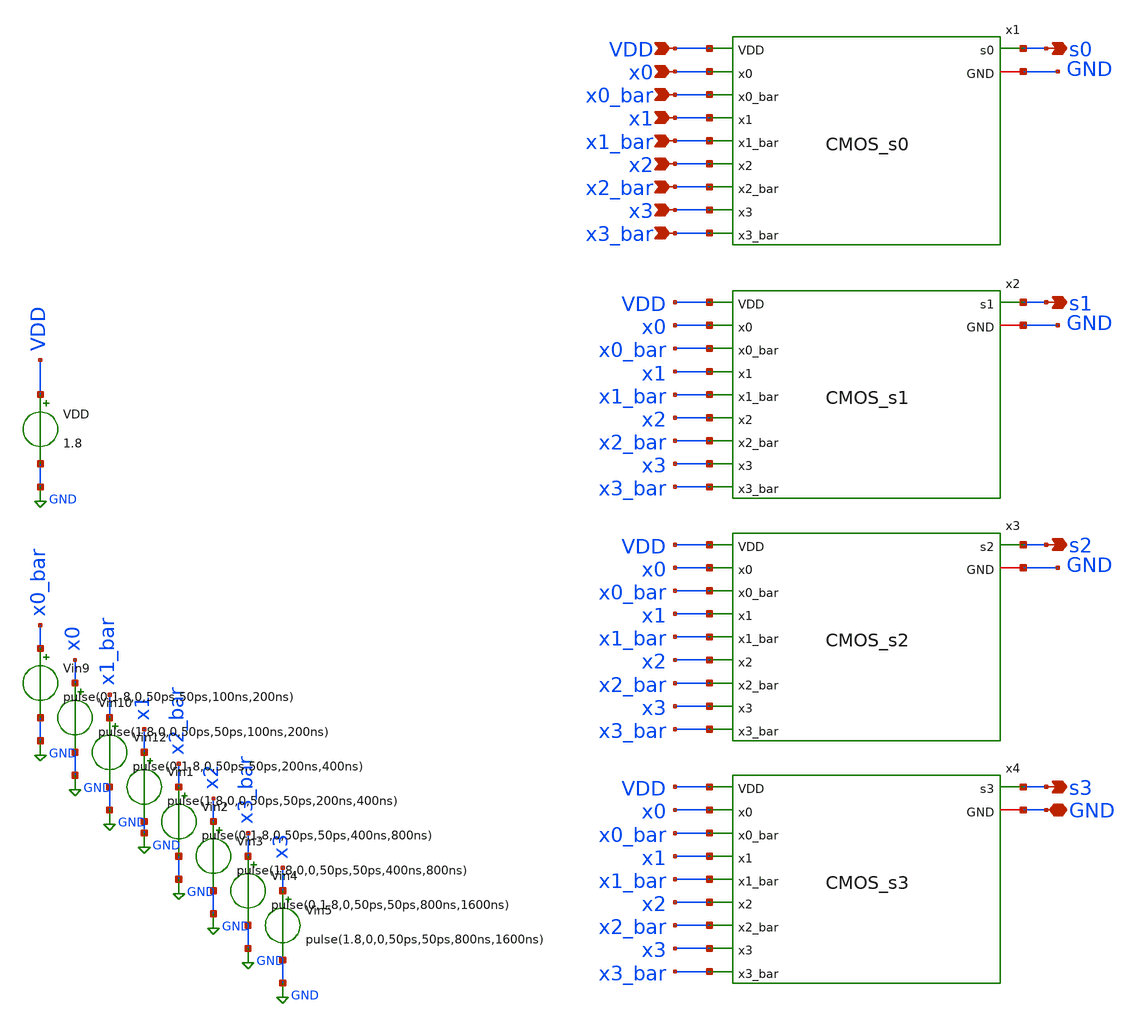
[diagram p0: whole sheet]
** sch_path: skywater_stuff/untitled-14.sch
**.subckt untitled-14 x0 x0_bar x1 x1_bar x2 x2_bar x3 x3_bar VDD GND s0 s1 s2 s3
*.ipin x0
*.ipin x0_bar
*.ipin x1
*.ipin x1_bar
*.ipin x2
*.ipin x2_bar
*.ipin x3
*.ipin x3_bar
*.ipin VDD
*.iopin GND
*.opin s0
*.opin s1
*.opin s2
*.opin s3
x1 GND x0 x0_bar x1 x1_bar x2 x2_bar x3 x3_bar VDD s0 CMOS_s0
x2 GND x0 x0_bar x1 x1_bar x2 x2_bar x3 VDD x3_bar s1 CMOS_s1
x3 GND x0 x0_bar x1 x1_bar x2 x2_bar x3 VDD x3_bar s2 CMOS_s2
x4 GND x0 x0_bar x1 x1_bar x2 x2_bar x3 VDD x3_bar s3 CMOS_s3
Vin9 x0_bar GND pulse(0,1.8,0,50ps,50ps,100ns,200ns)
Vin10 x0 GND pulse(1.8,0,0,50ps,50ps,100ns,200ns)
Vin12 x1_bar GND pulse(0,1.8,0,50ps,50ps,200ns,400ns)
Vin1 x1 GND pulse(1.8,0,0,50ps,50ps,200ns,400ns)
Vin2 x2_bar GND pulse(0,1.8,0,50ps,50ps,400ns,800ns)
Vin3 x2 GND pulse(1.8,0,0,50ps,50ps,400ns,800ns)
Vin4 x3_bar GND pulse(0,1.8,0,50ps,50ps,800ns,1600ns)
Vin5 x3 GND pulse(1.8,0,0,50ps,50ps,800ns,1600ns)
VDD VDD GND 1.8
**** begin user architecture code

.lib /research/pdk/open_pdks/share/pdk/sky130A/libs.tech/ngspice/sky130.lib.spice tt
.control
save all
tran 0.1n 10u
plot v(s0) v(s1) v(s2) v(s3)
plot v(s0)
plot v(s1)
plot v(s2)
plot v(s3)
let Pinst= v(VDD)*i(vVDD)
**let Pinst_CLK0_CLK2_Dis0_Dis2 =
*+ (v(CLK0)*i(vclk0))+(v(Dis0)*i(Vdis0))+(v(CLK1)*i(vclk1))+(v(Dis1)*i(Vdis1))+(v(CLK2)*i(vclk2))+(v(Dis2)*i(Vdis2))
**plot Pinst_CLK0
plot Pinst
**plot Pinst_CLK0_CLK2_Dis0_Dis2
wrdata CMOS_sbox_sim.raw Pinst s0 s1 s2 s3
wrdata CMOS_sim_Pinst_test.csv Pinst
.endc


**** end user architecture code
**.ends
.GLOBAL GND
.end
